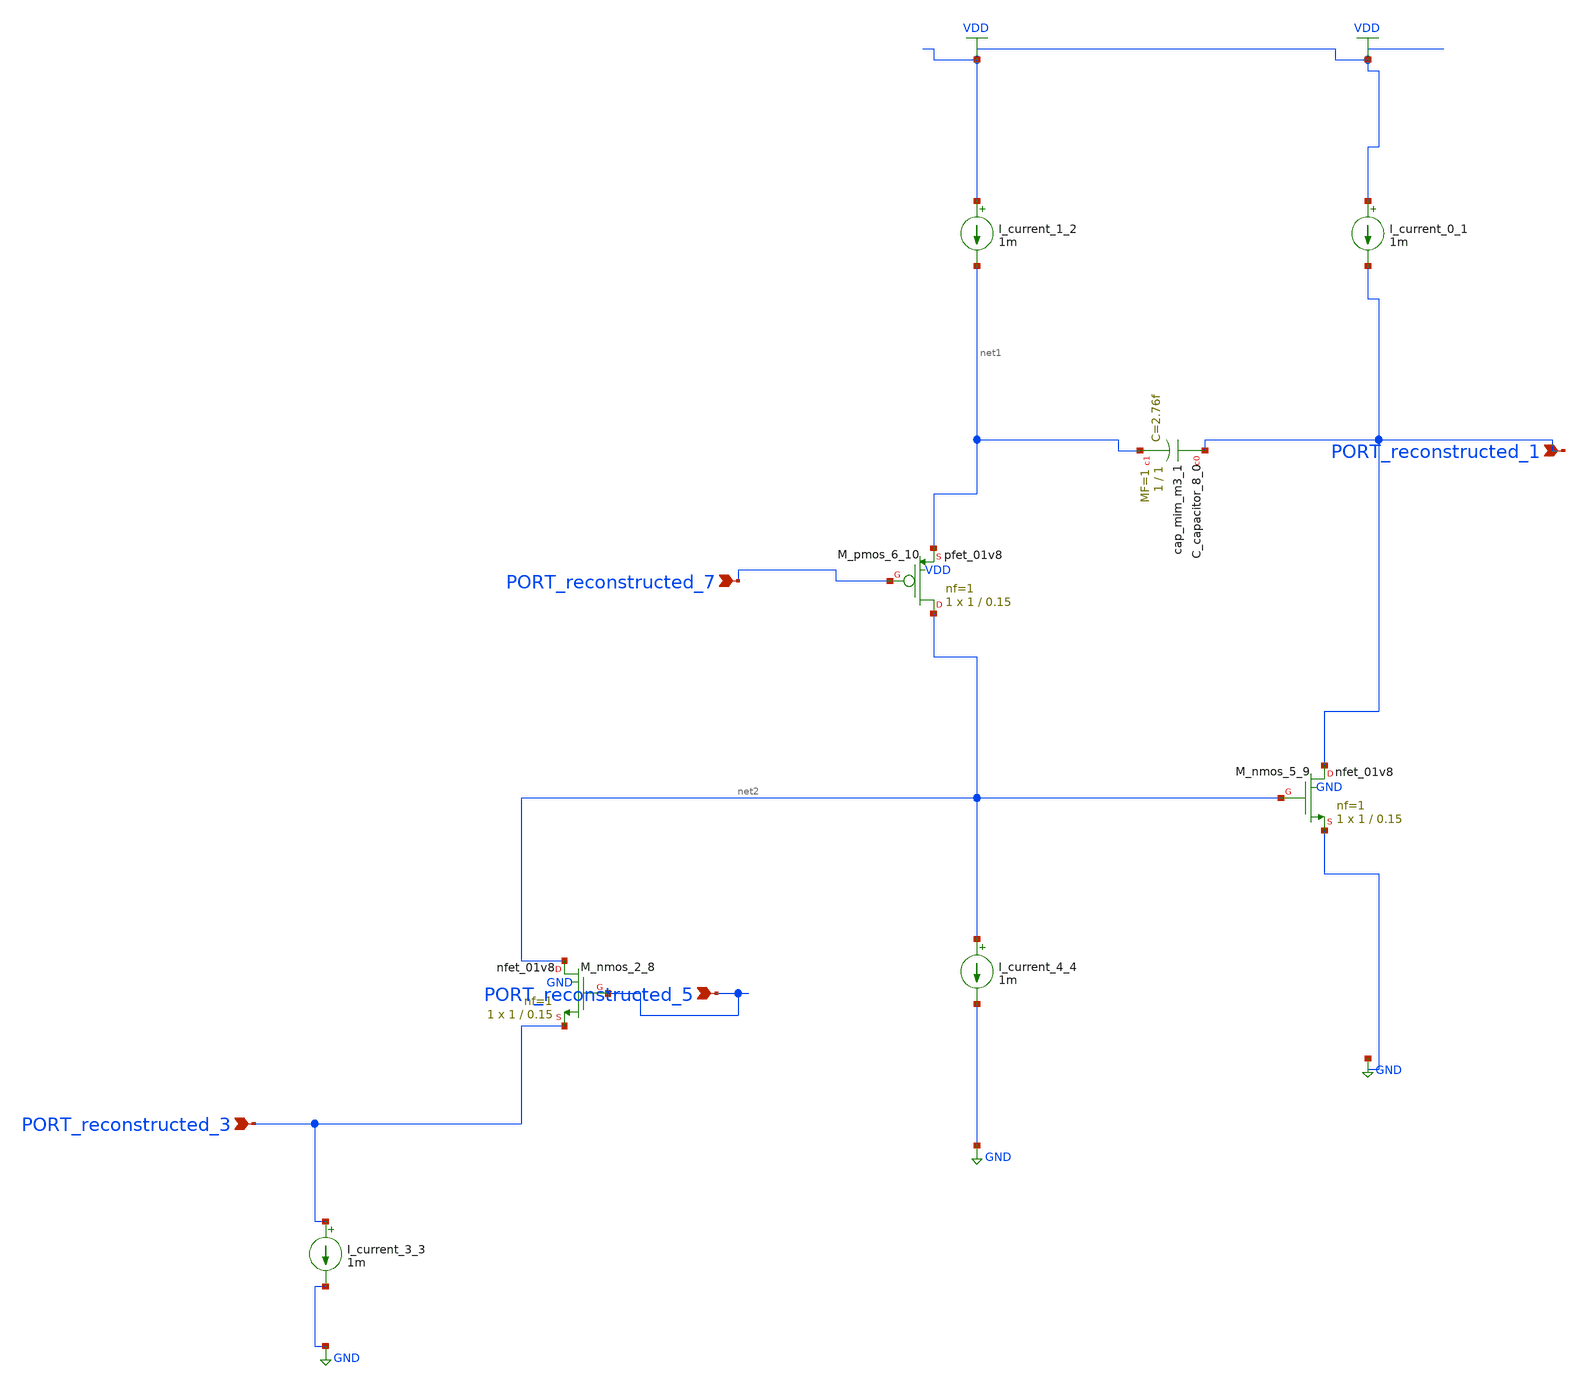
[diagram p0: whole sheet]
** sch_path: schematics/AMSNet/736.sch
**.subckt 736 PORT_reconstructed_7 PORT_reconstructed_1 PORT_reconstructed_5 PORT_reconstructed_3
*.ipin PORT_reconstructed_7
*.ipin PORT_reconstructed_1
*.ipin PORT_reconstructed_5
*.ipin PORT_reconstructed_3
XC_capacitor_8_0 PORT_reconstructed_1 net1 sky130_fd_pr__cap_mim_m3_1 W=1 L=1 MF=1 m=1
I_current_0_1 VDD PORT_reconstructed_1 1m
I_current_1_2 VDD net1 1m
I_current_3_3 PORT_reconstructed_3 GND 1m
I_current_4_4 net2 GND 1m
XM_nmos_2_8 net2 PORT_reconstructed_5 PORT_reconstructed_3 GND sky130_fd_pr__nfet_01v8 L=0.15 W=1 nf=1
+ ad='int((1 + 1)/2) * 1 / 1 * 0.29' as='int((1 + 2)/2) * 1 / 1 * 0.29' pd='2*int((1 + 1)/2) * (1 / 1 + 0.29)'
+ ps='2*int((1 + 2)/2) * (1 / 1 + 0.29)' nrd='0.29 / 1 ' nrs='0.29 / 1 ' sa=0 sb=0 sd=0 mult=1 m=1
XM_nmos_5_9 PORT_reconstructed_1 net2 GND GND sky130_fd_pr__nfet_01v8 L=0.15 W=1 nf=1 ad='int((1 + 1)/2) * 1 / 1 * 0.29'
+ as='int((1 + 2)/2) * 1 / 1 * 0.29' pd='2*int((1 + 1)/2) * (1 / 1 + 0.29)' ps='2*int((1 + 2)/2) * (1 / 1 + 0.29)'
+ nrd='0.29 / 1 ' nrs='0.29 / 1 ' sa=0 sb=0 sd=0 mult=1 m=1
XM_pmos_6_10 net2 PORT_reconstructed_7 net1 VDD sky130_fd_pr__pfet_01v8 L=0.15 W=1 nf=1 ad='int((1 + 1)/2) * 1 / 1 * 0.29'
+ as='int((1 + 2)/2) * 1 / 1 * 0.29' pd='2*int((1 + 1)/2) * (1 / 1 + 0.29)' ps='2*int((1 + 2)/2) * (1 / 1 + 0.29)'
+ nrd='0.29 / 1 ' nrs='0.29 / 1 ' sa=0 sb=0 sd=0 mult=1 m=1
**.ends
.GLOBAL GND
.GLOBAL VDD
.end
